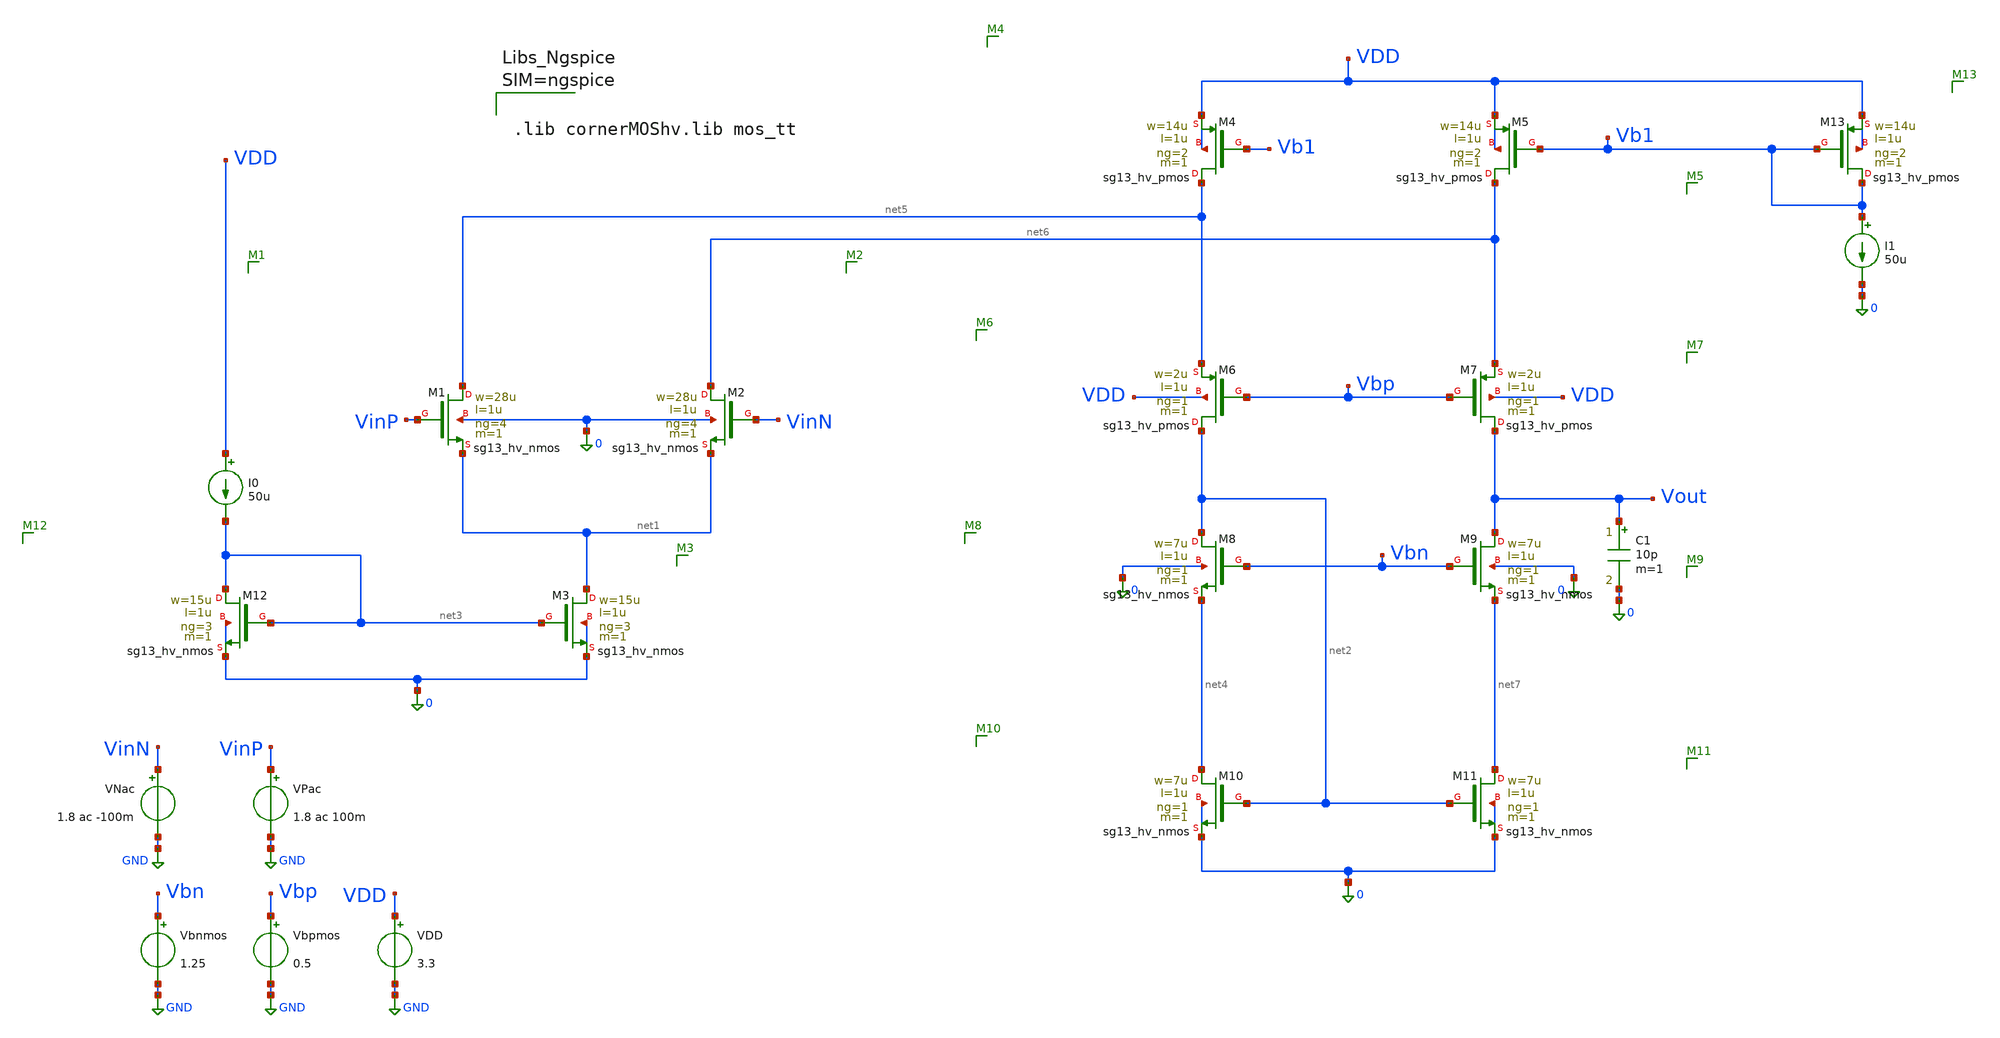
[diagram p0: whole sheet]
** sch_path: v1_ideal_current_sources/op/OP-foldedOTA.sch
**.subckt OP-foldedOTA
XM1 net5 VinP net1 0 sg13_hv_nmos w=28u l=1u ng=4 m=1 mm_ok=1
XM2 net6 VinN net1 0 sg13_hv_nmos w=28u l=1u ng=4 m=1 mm_ok=1
XM3 net1 net3 0 0 sg13_hv_nmos w=15u l=1u ng=3 m=1 mm_ok=1
XM4 net5 Vb1 VDD VDD sg13_hv_pmos w=14u l=1u ng=2 m=1 mm_ok=1
XM5 net6 Vb1 VDD VDD sg13_hv_pmos w=14u l=1u ng=2 m=1 mm_ok=1
XM6 net2 Vbp net5 VDD sg13_hv_pmos w=2u l=1u ng=1 m=1 mm_ok=1
XM7 Vout Vbp net6 VDD sg13_hv_pmos w=2u l=1u ng=1 m=1 mm_ok=1
XM8 net2 Vbn net4 0 sg13_hv_nmos w=7u l=1u ng=1 m=1 mm_ok=1
XM9 Vout Vbn net7 0 sg13_hv_nmos w=7u l=1u ng=1 m=1 mm_ok=1
XM10 net4 net2 0 0 sg13_hv_nmos w=7u l=1u ng=1 m=1 mm_ok=1
XM11 net7 net2 0 0 sg13_hv_nmos w=7u l=1u ng=1 m=1 mm_ok=1
XM12 net3 net3 0 0 sg13_hv_nmos w=15u l=1u ng=3 m=1 mm_ok=1
I0 VDD net3 50u
XM13 Vb1 Vb1 VDD VDD sg13_hv_pmos w=14u l=1u ng=2 m=1 mm_ok=1
I1 Vb1 0 50u
VPac VinP GND 1.8 ac 100m
VNac VinN GND 1.8 ac -100m
Vbnmos Vbn GND 1.25
Vbpmos Vbp GND 0.5
C1 Vout 0 10p m=1
VDD VDD GND 3.3
**** begin user architecture code



.lib cornerMOShv.lib mos_tt





.include OP-foldedOTA.save
.control
op
write OP-foldedOTA.raw
.endc


**** end user architecture code
**.ends
.GLOBAL GND
.end
